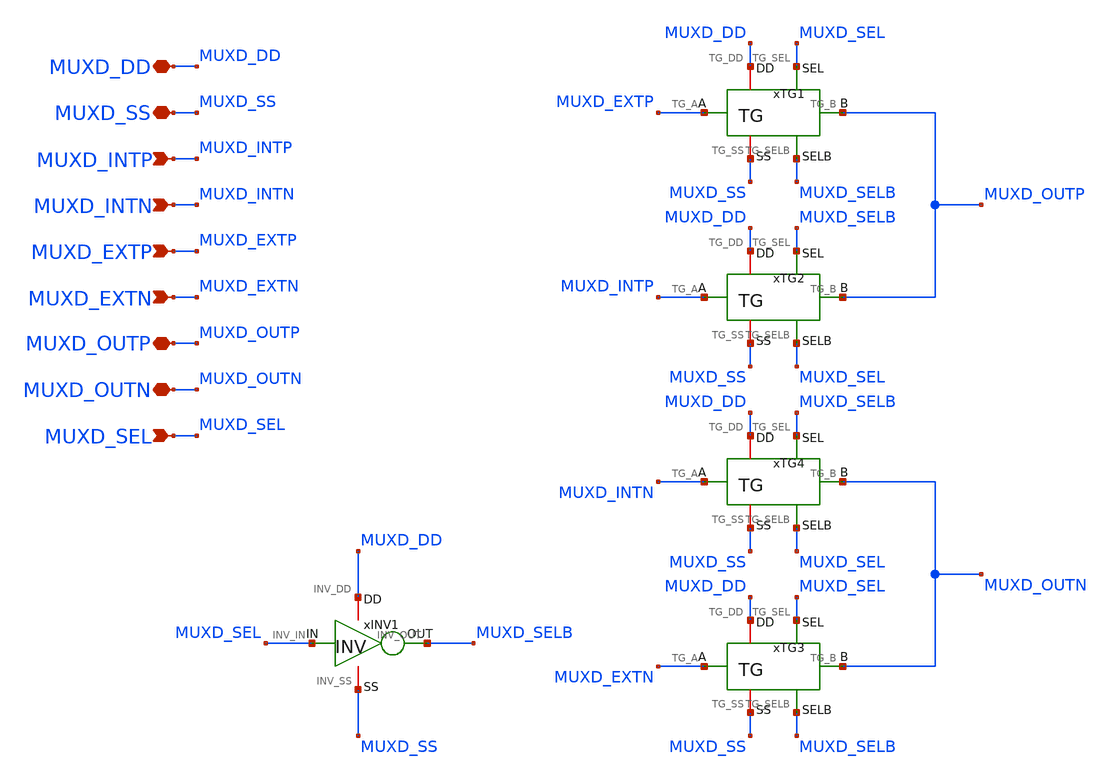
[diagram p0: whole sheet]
** sch_path: Design_Files/IC Design/Schematic/DIGITAL_BLOCKS/MUXD/MUXD.sch
**.subckt MUXD MUXD_DD MUXD_SS MUXD_INTP MUXD_INTN MUXD_OUTP MUXD_OUTN MUXD_EXTP MUXD_EXTN MUXD_SEL
*.iopin MUXD_DD
*.iopin MUXD_SS
*.ipin MUXD_INTP
*.ipin MUXD_INTN
*.iopin MUXD_OUTP
*.iopin MUXD_OUTN
*.ipin MUXD_EXTP
*.ipin MUXD_EXTN
*.ipin MUXD_SEL
xINV1 MUXD_DD MUXD_SS MUXD_SEL MUXD_SELB INV
xTG1 MUXD_DD MUXD_SS MUXD_EXTP MUXD_OUTP MUXD_SEL MUXD_SELB TG
xTG2 MUXD_DD MUXD_SS MUXD_INTP MUXD_OUTP MUXD_SELB MUXD_SEL TG
xTG3 MUXD_DD MUXD_SS MUXD_EXTN MUXD_OUTN MUXD_SEL MUXD_SELB TG
xTG4 MUXD_DD MUXD_SS MUXD_INTN MUXD_OUTN MUXD_SELB MUXD_SEL TG
**.ends

* expanding   symbol:  ECG_Acquisition_IC/Design_Files/IC
*+ Design/Schematic/DIGITAL_BLOCKS/INV/INV.sym # of pins=4
** sym_path: Design_Files/IC Design/Schematic/INV/INV.sym
** sch_path: Design_Files/IC Design/Schematic/INV/INV.sch
.subckt INV INV_DD INV_SS INV_IN INV_OUT
*.iopin INV_DD
*.iopin INV_SS
*.ipin INV_IN
*.opin INV_OUT
XMINVP INV_OUT INV_IN INV_DD INV_DD pfet_03v3 L=0.5u W=2u nf=1 ad='int((nf+1)/2) * W/nf * 0.18u' as='int((nf+2)/2) * W/nf * 0.18u'
+ pd='2*int((nf+1)/2) * (W/nf + 0.18u)' ps='2*int((nf+2)/2) * (W/nf + 0.18u)' nrd='0.18u / W' nrs='0.18u / W'
+ sa=0 sb=0 sd=0 m=1
XMINVN INV_OUT INV_IN INV_SS INV_SS nfet_03v3 L=0.5u W=1u nf=1 ad='int((nf+1)/2) * W/nf * 0.18u' as='int((nf+2)/2) * W/nf * 0.18u'
+ pd='2*int((nf+1)/2) * (W/nf + 0.18u)' ps='2*int((nf+2)/2) * (W/nf + 0.18u)' nrd='0.18u / W' nrs='0.18u / W'
+ sa=0 sb=0 sd=0 m=1
.ends


* expanding   symbol:  ECG_Acquisition_IC/Design_Files/IC Design/Schematic/DIGITAL_BLOCKS/TG/TG.sym
*+ # of pins=6
** sym_path: Design_Files/IC Design/Schematic/TG/TG.sym
** sch_path: Design_Files/IC Design/Schematic/TG/TG.sch
.subckt TG TG_DD TG_SS TG_A TG_B TG_SEL TG_SELB
*.iopin TG_DD
*.iopin TG_SS
*.iopin TG_A
*.iopin TG_B
*.ipin TG_SEL
*.ipin TG_SELB
XMTGP TG_B TG_SELB TG_A TG_DD pfet_03v3 L=0.5u W=40u nf=1 ad='int((nf+1)/2) * W/nf * 0.18u' as='int((nf+2)/2) * W/nf * 0.18u'
+ pd='2*int((nf+1)/2) * (W/nf + 0.18u)' ps='2*int((nf+2)/2) * (W/nf + 0.18u)' nrd='0.18u / W' nrs='0.18u / W'
+ sa=0 sb=0 sd=0 m=1
XMTGN TG_A TG_SEL TG_B TG_SS nfet_03v3 L=0.5u W=20u nf=1 ad='int((nf+1)/2) * W/nf * 0.18u' as='int((nf+2)/2) * W/nf * 0.18u'
+ pd='2*int((nf+1)/2) * (W/nf + 0.18u)' ps='2*int((nf+2)/2) * (W/nf + 0.18u)' nrd='0.18u / W' nrs='0.18u / W'
+ sa=0 sb=0 sd=0 m=1
.ends

.end
